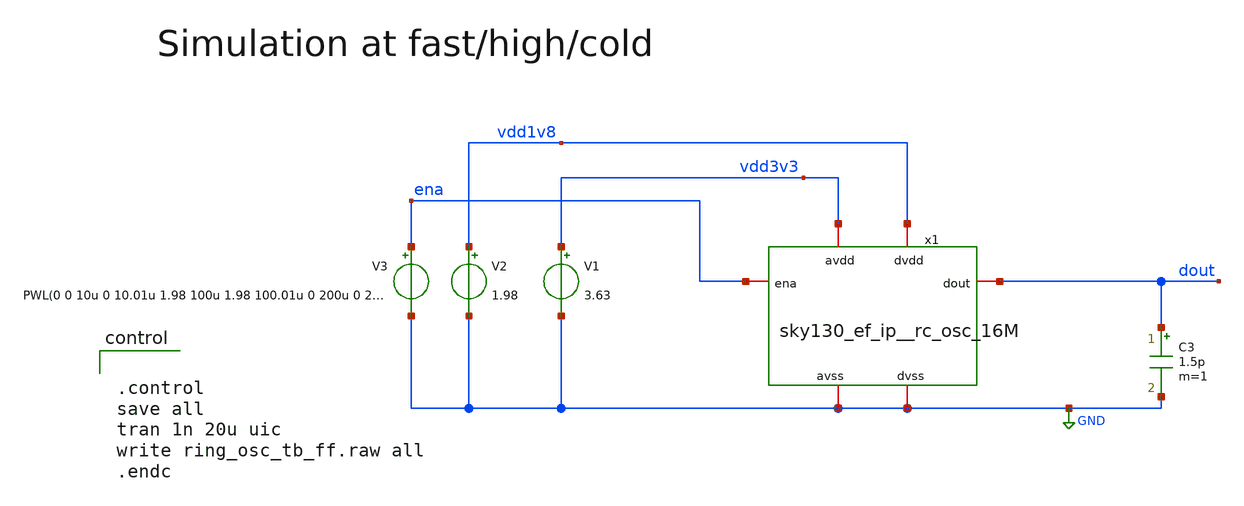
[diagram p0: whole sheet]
** sch_path: cace/templates/ring_osc_tb_ff.sch
**.subckt ring_osc_tb_ff
x1 ena vdd1v8 vdd3v3 GND GND dout sky130_ef_ip__rc_osc_16M
V1 vdd3v3 GND 3.63
V2 vdd1v8 GND 1.98
C3 dout GND 1.5p m=1
V3 ena GND PWL(0 0 10u 0 10.01u 1.98 100u 1.98 100.01u 0 200u 0 200.01u 1.98)
**** begin user architecture code


.option TEMP=-40
.lib /usr/share/pdk/sky130A/libs.tech/ngspice/sky130.lib.spice ff




.control
save all
tran 1n 20u uic
write ring_osc_tb_ff.raw all
.endc


**** end user architecture code
**.ends
.GLOBAL GND
.end
